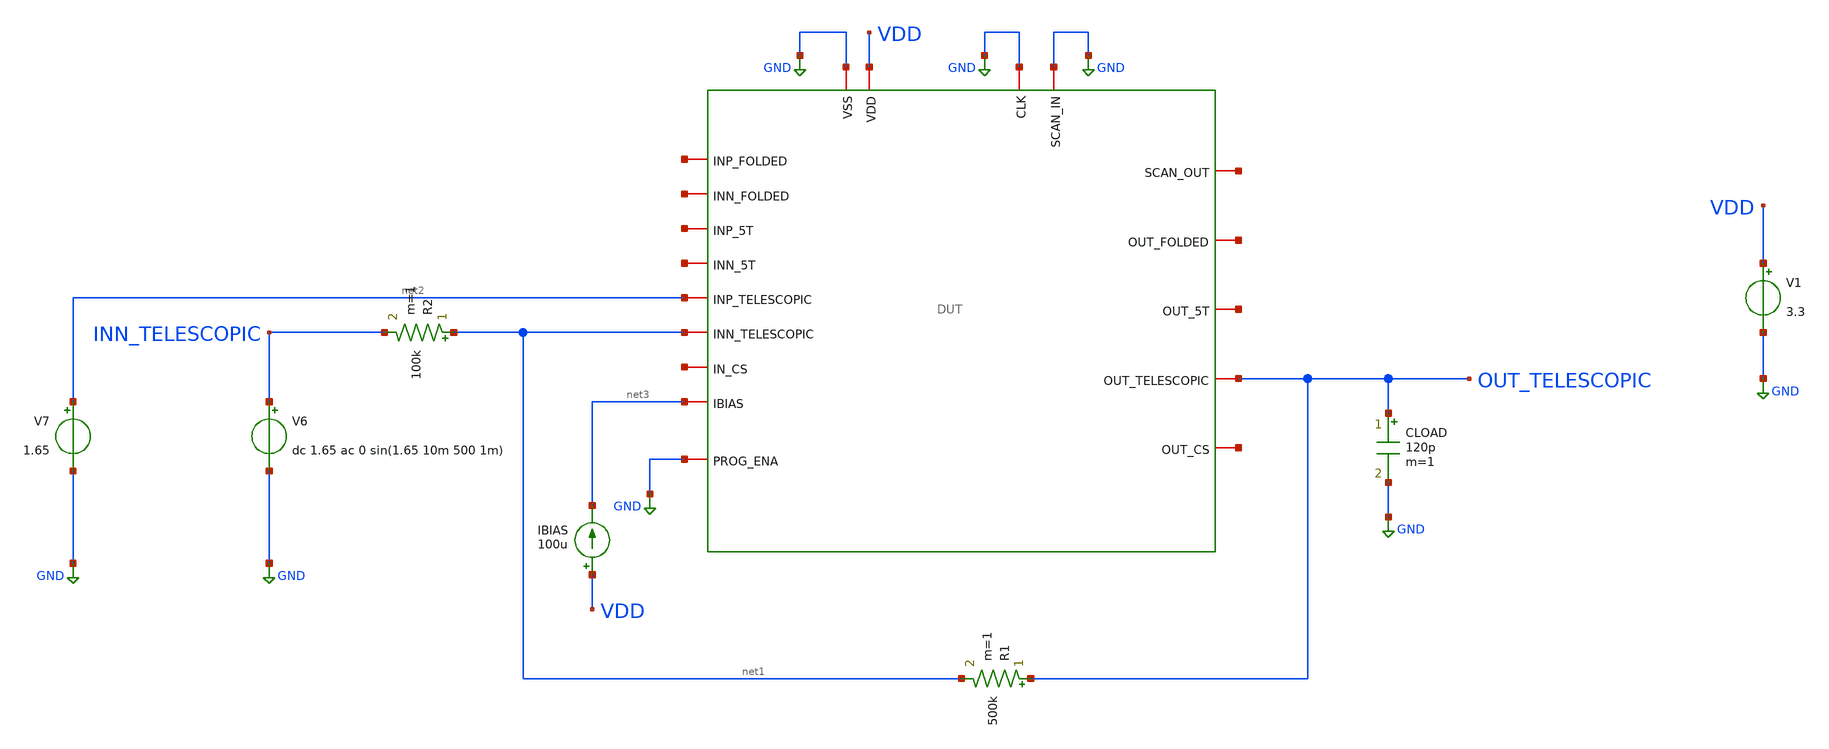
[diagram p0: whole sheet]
** sch_path: designs/libs/verification/start_up_cir/tele/default_inverting_telescopic.sch
**.subckt default_inverting_telescopic
V1 VDD GND 3.3
CLOAD OUT_TELESCOPIC GND 120p m=1
R1 OUT_TELESCOPIC net1 500k m=1
R2 net1 INN_TELESCOPIC 100k m=1
V6 INN_TELESCOPIC GND dc 1.65 ac 0 sin(1.65 10m 500 1m)
V7 net2 GND 1.65
IBIAS VDD net3 100u
x1 GND net4 GND GND VDD net5 net6 net7 net3 net8 net9 net10 net2 OUT_TELESCOPIC net11 net12 net1 GND
+ DUT
**** begin user architecture code

.include $::180MCU_MODELS/design.ngspice
.lib $::180MCU_MODELS/sm141064.ngspice typical




.include /foss/designs/libs/pex/DUT.spice
.control
tran 1u 5m

plot v(out_telescopic) v(inn_telescopic)
wrdata /foss/designs/libs/verification/start_up_cir/tele/default.csv v(out_telescopic)
+ v(inn_telescopic)

meas tran vout_pp pp v(out_telescopic) from=2m to=5m
meas tran vin_pp pp v(inn_telescopic) from=2m to=5m
let gain = vout_pp / vin_pp
print gain

meas tran vout_dc avg v(out_telescopic) from=2m to=5m
meas tran vin_dc avg v(inn_telescopic) from=2m to=5m
let dc_offset = vout_dc - vin_dc
let input_offset = dc_offset / 6
print vout_dc vin_dc dc_offset input_offset

let ideal_gain = 5
let gain_error_pct = (ideal_gain - gain) / ideal_gain * 100
print gain_error_pct

meas tran idd avg i(v1) from=2m to=5m
let power = abs(idd) * 3.3
print idd power
.endc


**** end user architecture code
**.ends
.GLOBAL GND
.end
